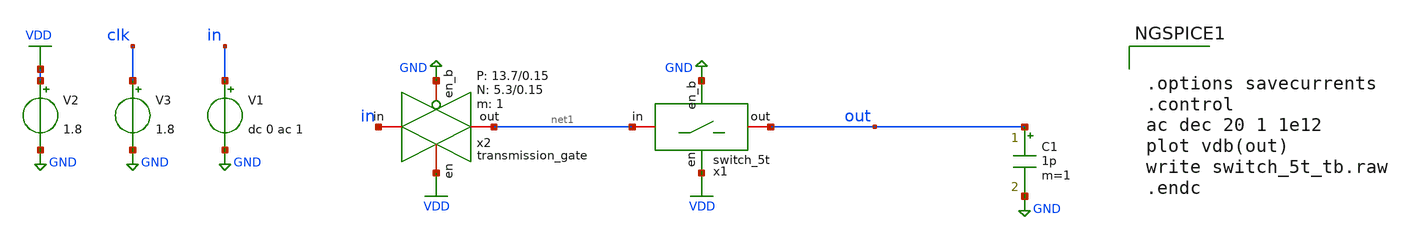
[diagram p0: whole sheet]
** sch_path: verification/analog_modulator/switch_5t_tb.sch
**.subckt switch_5t_tb
V2 VDD GND 1.8
V3 clk GND 1.8
V1 in GND dc 0 ac 1
x1 net1 out VDD GND VDD GND switch_5t
C1 out GND 1p m=1
x2 in net1 VDD GND VDD VSS 1 5.3 0.15 13.7 0.15 transmission_gate
**** begin user architecture code


.options savecurrents
.control
ac dec 20 1 1e12
plot vdb(out)
write switch_5t_tb.raw
.endc



** opencircuitdesign pdks install
.lib /farmshare/home/classes/ee/372/PDKs/open_pdks_1.0.310/sky130/sky130A/libs.tech/ngspice/sky130.lib.spice tt
.inc /farmshare/home/classes/ee/372/PDKs/open_pdks_1.0.310/sky130/sky130A/libs.ref/sky130_fd_sc_hd/spice/sky130_fd_sc_hd.spice

**** end user architecture code
**.ends

* expanding   symbol:  switch_5t.sym # of pins=4
** sym_path: design/analog_modulator/schematic/switch_5t.sym
** sch_path: design/analog_modulator/schematic/switch_5t.sch
.subckt switch_5t in out en en_b VDD VSS
*.iopin in
*.iopin out
*.ipin en
*.ipin en_b
x1 in net1 en en_b VDD VSS 1 5.3 0.15 13.7 0.15 transmission_gate
x2 net1 out en en_b VDD VSS 1 5.3 0.15 13.7 0.15 transmission_gate
XM1 net1 en_b VSS VSS sky130_fd_pr__nfet_01v8 L=0.15 W=0.5 nf=1 ad='int((nf+1)/2) * W/nf * 0.29' as='int((nf+2)/2) * W/nf * 0.29'
+ pd='2*int((nf+1)/2) * (W/nf + 0.29)' ps='2*int((nf+2)/2) * (W/nf + 0.29)' nrd='0.29 / W' nrs='0.29 / W'
+ sa=0 sb=0 sd=0 mult=1 m=1
.ends


* expanding   symbol:  transmission_gate.sym # of pins=4
** sym_path: design/schematic/transmission_gate.sym
** sch_path: design/schematic/transmission_gate.sch
.subckt transmission_gate in out en en_b VDD VSS N W_N L_N W_P L_P    N=1 W_N=5.3 L_N=0.15 W_P=13.7
+ L_P=0.15
*.iopin in
*.iopin out
*.ipin en
*.ipin en_b
XM1 out en in VSS sky130_fd_pr__nfet_01v8 L=L_N W=W_N nf=1 ad='int((nf+1)/2) * W/nf * 0.29' as='int((nf+2)/2) * W/nf * 0.29'
+ pd='2*int((nf+1)/2) * (W/nf + 0.29)' ps='2*int((nf+2)/2) * (W/nf + 0.29)' nrd='0.29 / W' nrs='0.29 / W'
+ sa=0 sb=0 sd=0 mult=N m=N
XM2 out en_b in VDD sky130_fd_pr__pfet_01v8 L=L_P W=W_P nf=1 ad='int((nf+1)/2) * W/nf * 0.29' as='int((nf+2)/2) * W/nf * 0.29'
+ pd='2*int((nf+1)/2) * (W/nf + 0.29)' ps='2*int((nf+2)/2) * (W/nf + 0.29)' nrd='0.29 / W' nrs='0.29 / W'
+ sa=0 sb=0 sd=0 mult=N m=N
.ends

.GLOBAL GND
.GLOBAL VDD
.end
